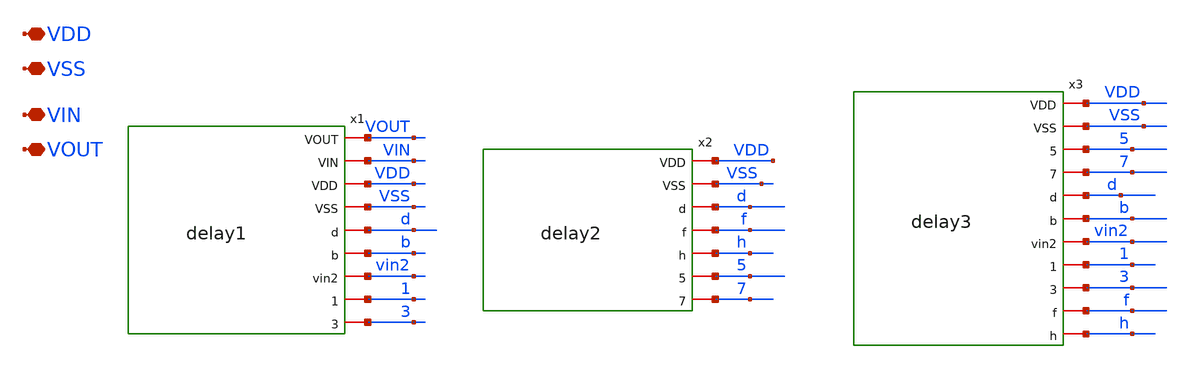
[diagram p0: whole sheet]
** sch_path: xschem/DC_DC_Converter_xschem/DC_DC_Converter/Delay_block_revised/delay1_delay2_delay3.sch
**.subckt delay1_delay2_delay3 VDD VSS VIN VOUT
*.iopin VDD
*.iopin VSS
*.iopin VIN
*.iopin VOUT
x1 VOUT VIN VDD VSS d b vin2 1 3 delay1
x2 VDD VSS d f h 5 7 delay2
x3 VDD VSS 5 7 d b vin2 1 3 f h delay3
**.ends
.end
